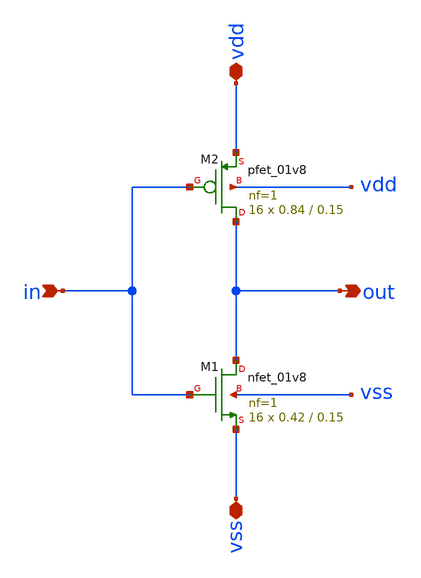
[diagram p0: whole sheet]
** sch_path: xschem/inverter_min_x16.sch
**.subckt inverter_min_x16 vss in out vdd
*.iopin vss
*.ipin in
*.opin out
*.iopin vdd
XM2 out in vdd vdd sky130_fd_pr__pfet_01v8 L=0.15 W=0.84 nf=1 ad='int((nf+1)/2) * W/nf * 0.29' as='int((nf+2)/2) * W/nf * 0.29'
+ pd='2*int((nf+1)/2) * (W/nf + 0.29)' ps='2*int((nf+2)/2) * (W/nf + 0.29)' nrd='0.29 / W' nrs='0.29 / W'
+ sa=0 sb=0 sd=0 mult=16 m=16
XM1 out in vss vss sky130_fd_pr__nfet_01v8 L=0.15 W=0.42 nf=1 ad='int((nf+1)/2) * W/nf * 0.29' as='int((nf+2)/2) * W/nf * 0.29'
+ pd='2*int((nf+1)/2) * (W/nf + 0.29)' ps='2*int((nf+2)/2) * (W/nf + 0.29)' nrd='0.29 / W' nrs='0.29 / W'
+ sa=0 sb=0 sd=0 mult=16 m=16
**.ends
.end
